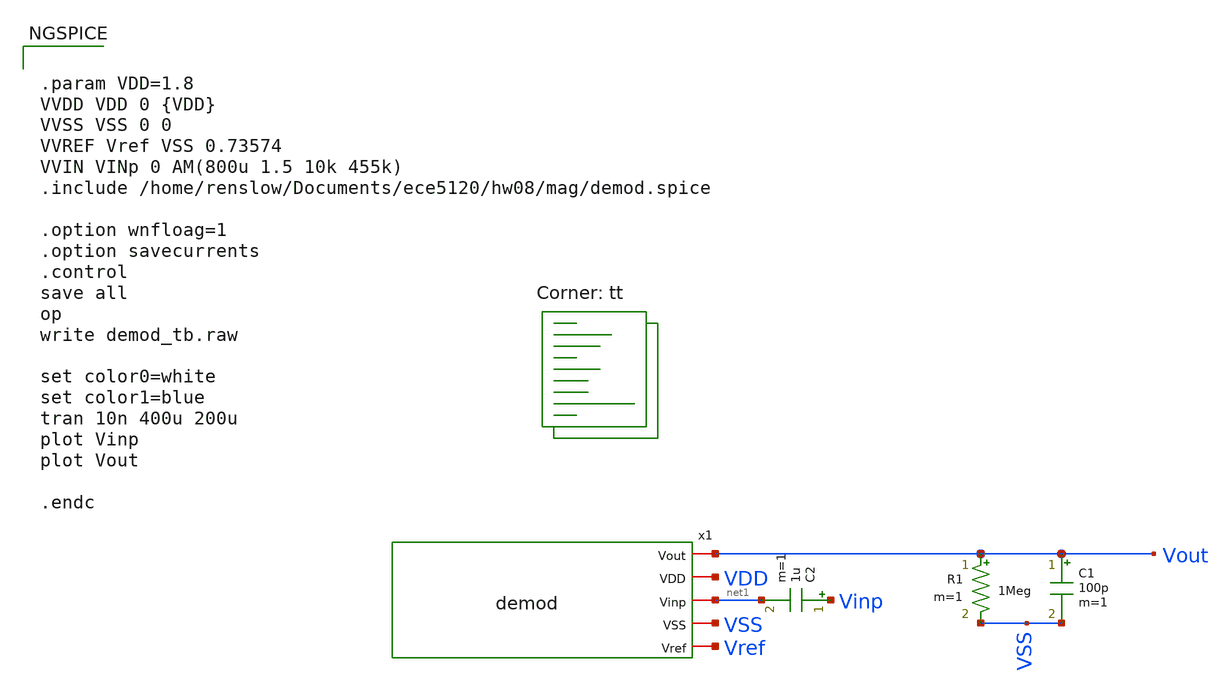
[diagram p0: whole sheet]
** sch_path: hw08/mag/demod_tb.sch
**.subckt demod_tb
x1 Vout VDD net1 VSS Vref demod
R1 Vout VSS 1Meg m=1
C1 Vout VSS 100p m=1
C2 Vinp net1 1u m=1
**** begin user architecture code
.lib $::SKYWATER_MODELS/sky130.lib.spice tt


.param VDD=1.8
VVDD VDD 0 {VDD}
VVSS VSS 0 0
VVREF Vref VSS 0.73574
VVIN VINp 0 AM(800u 1.5 10k 455k)
.include /home/renslow/Documents/ece5120/hw08/mag/demod.spice

.option wnfloag=1
.option savecurrents
.control
save all
op
write demod_tb.raw

set color0=white
set color1=blue
tran 10n 400u 200u
plot Vinp
plot Vout

.endc


**** end user architecture code
**.ends
.end
